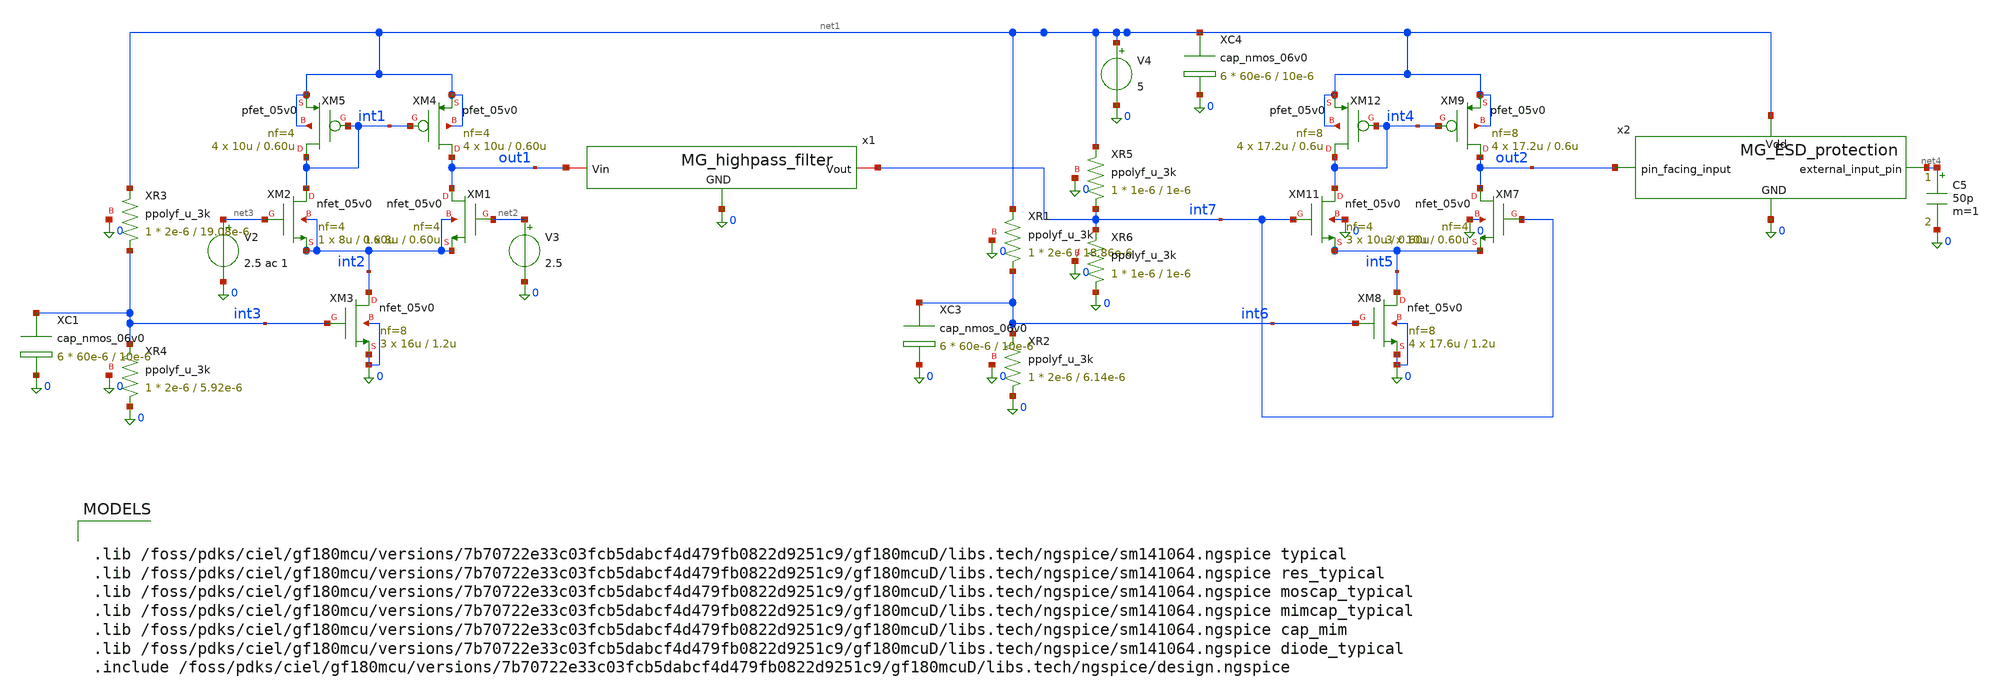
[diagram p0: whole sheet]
** sch_path: MRTMOS_final_chip/gm2+gm3_tb.sch
**.subckt gm2+gm3_tb
XM1 out1 net2 int2 int2 nfet_05v0 L=0.60u W=8u nf=4 ad='int((nf+1)/2) * W/nf * 0.18u' as='int((nf+2)/2) * W/nf * 0.18u'
+ pd='2*int((nf+1)/2) * (W/nf + 0.18u)' ps='2*int((nf+2)/2) * (W/nf + 0.18u)' nrd='0.18u / W' nrs='0.18u / W'
+ sa=0 sb=0 sd=0 m=1
XM2 int1 net3 int2 int2 nfet_05v0 L=0.60u W=8u nf=4 ad='int((nf+1)/2) * W/nf * 0.18u' as='int((nf+2)/2) * W/nf * 0.18u'
+ pd='2*int((nf+1)/2) * (W/nf + 0.18u)' ps='2*int((nf+2)/2) * (W/nf + 0.18u)' nrd='0.18u / W' nrs='0.18u / W'
+ sa=0 sb=0 sd=0 m=1
XM3 int2 int3 0 0 nfet_05v0 L=1.2u W=16u nf=8 ad='int((nf+1)/2) * W/nf * 0.18u' as='int((nf+2)/2) * W/nf * 0.18u'
+ pd='2*int((nf+1)/2) * (W/nf + 0.18u)' ps='2*int((nf+2)/2) * (W/nf + 0.18u)' nrd='0.18u / W' nrs='0.18u / W'
+ sa=0 sb=0 sd=0 m=3
XM4 out1 int1 net1 net1 pfet_05v0 L=0.60u W=10u nf=4 ad='int((nf+1)/2) * W/nf * 0.18u' as='int((nf+2)/2) * W/nf * 0.18u'
+ pd='2*int((nf+1)/2) * (W/nf + 0.18u)' ps='2*int((nf+2)/2) * (W/nf + 0.18u)' nrd='0.18u / W' nrs='0.18u / W'
+ sa=0 sb=0 sd=0 m=4
XM5 int1 int1 net1 net1 pfet_05v0 L=0.60u W=10u nf=4 ad='int((nf+1)/2) * W/nf * 0.18u' as='int((nf+2)/2) * W/nf * 0.18u'
+ pd='2*int((nf+1)/2) * (W/nf + 0.18u)' ps='2*int((nf+2)/2) * (W/nf + 0.18u)' nrd='0.18u / W' nrs='0.18u / W'
+ sa=0 sb=0 sd=0 m=4
V2 net3 0 2.5 ac 1
V3 net2 0 2.5
XM7 out2 int7 int5 0 nfet_05v0 L=0.60u W=10u nf=4 ad='int((nf+1)/2) * W/nf * 0.18u' as='int((nf+2)/2) * W/nf * 0.18u'
+ pd='2*int((nf+1)/2) * (W/nf + 0.18u)' ps='2*int((nf+2)/2) * (W/nf + 0.18u)' nrd='0.18u / W' nrs='0.18u / W'
+ sa=0 sb=0 sd=0 m=3
XM8 int5 int6 0 0 nfet_05v0 L=1.2u W=17.6u nf=8 ad='int((nf+1)/2) * W/nf * 0.18u' as='int((nf+2)/2) * W/nf * 0.18u'
+ pd='2*int((nf+1)/2) * (W/nf + 0.18u)' ps='2*int((nf+2)/2) * (W/nf + 0.18u)' nrd='0.18u / W' nrs='0.18u / W'
+ sa=0 sb=0 sd=0 m=4
XM9 out2 int4 net1 net1 pfet_05v0 L=0.6u W=17.2u nf=8 ad='int((nf+1)/2) * W/nf * 0.18u' as='int((nf+2)/2) * W/nf * 0.18u'
+ pd='2*int((nf+1)/2) * (W/nf + 0.18u)' ps='2*int((nf+2)/2) * (W/nf + 0.18u)' nrd='0.18u / W' nrs='0.18u / W'
+ sa=0 sb=0 sd=0 m=4
V4 net1 0 5
XM11 int4 int7 int5 0 nfet_05v0 L=0.60u W=10u nf=4 ad='int((nf+1)/2) * W/nf * 0.18u' as='int((nf+2)/2) * W/nf * 0.18u'
+ pd='2*int((nf+1)/2) * (W/nf + 0.18u)' ps='2*int((nf+2)/2) * (W/nf + 0.18u)' nrd='0.18u / W' nrs='0.18u / W'
+ sa=0 sb=0 sd=0 m=3
XM12 int4 int4 net1 net1 pfet_05v0 L=0.6u W=17.2u nf=8 ad='int((nf+1)/2) * W/nf * 0.18u' as='int((nf+2)/2) * W/nf * 0.18u'
+ pd='2*int((nf+1)/2) * (W/nf + 0.18u)' ps='2*int((nf+2)/2) * (W/nf + 0.18u)' nrd='0.18u / W' nrs='0.18u / W'
+ sa=0 sb=0 sd=0 m=4
XR1 int6 net1 0 ppolyf_u_3k r_width=2e-6 r_length=18.86e-6 m=1
XR2 0 int6 0 ppolyf_u_3k r_width=2e-6 r_length=6.14e-6 m=1
XR3 int3 net1 0 ppolyf_u_3k r_width=2e-6 r_length=19.08e-6 m=1
XR4 0 int3 0 ppolyf_u_3k r_width=2e-6 r_length=5.92e-6 m=1
XR5 int7 net1 0 ppolyf_u_3k r_width=1e-6 r_length=1e-6 m=1
XR6 0 int7 0 ppolyf_u_3k r_width=1e-6 r_length=1e-6 m=1
x1 out1 int7 0 MG_highpass_filter
XC3 int6 0 cap_nmos_06v0 c_width=60e-6 c_length=10e-6 m=6
XC1 int3 0 cap_nmos_06v0 c_width=60e-6 c_length=10e-6 m=6
XC4 net1 0 cap_nmos_06v0 c_width=60e-6 c_length=10e-6 m=6
x2 net1 net4 out2 0 MG_ESD_protection
C5 net4 0 50p m=1
**** begin user architecture code


.lib /foss/pdks/ciel/gf180mcu/versions/7b70722e33c03fcb5dabcf4d479fb0822d9251c9/gf180mcuD/libs.tech/ngspice/sm141064.ngspice typical
.lib /foss/pdks/ciel/gf180mcu/versions/7b70722e33c03fcb5dabcf4d479fb0822d9251c9/gf180mcuD/libs.tech/ngspice/sm141064.ngspice res_typical
.lib /foss/pdks/ciel/gf180mcu/versions/7b70722e33c03fcb5dabcf4d479fb0822d9251c9/gf180mcuD/libs.tech/ngspice/sm141064.ngspice moscap_typical
.lib /foss/pdks/ciel/gf180mcu/versions/7b70722e33c03fcb5dabcf4d479fb0822d9251c9/gf180mcuD/libs.tech/ngspice/sm141064.ngspice mimcap_typical
.lib /foss/pdks/ciel/gf180mcu/versions/7b70722e33c03fcb5dabcf4d479fb0822d9251c9/gf180mcuD/libs.tech/ngspice/sm141064.ngspice cap_mim
.lib /foss/pdks/ciel/gf180mcu/versions/7b70722e33c03fcb5dabcf4d479fb0822d9251c9/gf180mcuD/libs.tech/ngspice/sm141064.ngspice diode_typical
.include /foss/pdks/ciel/gf180mcu/versions/7b70722e33c03fcb5dabcf4d479fb0822d9251c9/gf180mcuD/libs.tech/ngspice/design.ngspice




.control
  	save all

	ac dec 20 1 100Meg
	remzerovec
	write gm1+gm3_test_ac.raw
.endc

.options savecurrents


**** end user architecture code
**.ends
.end
